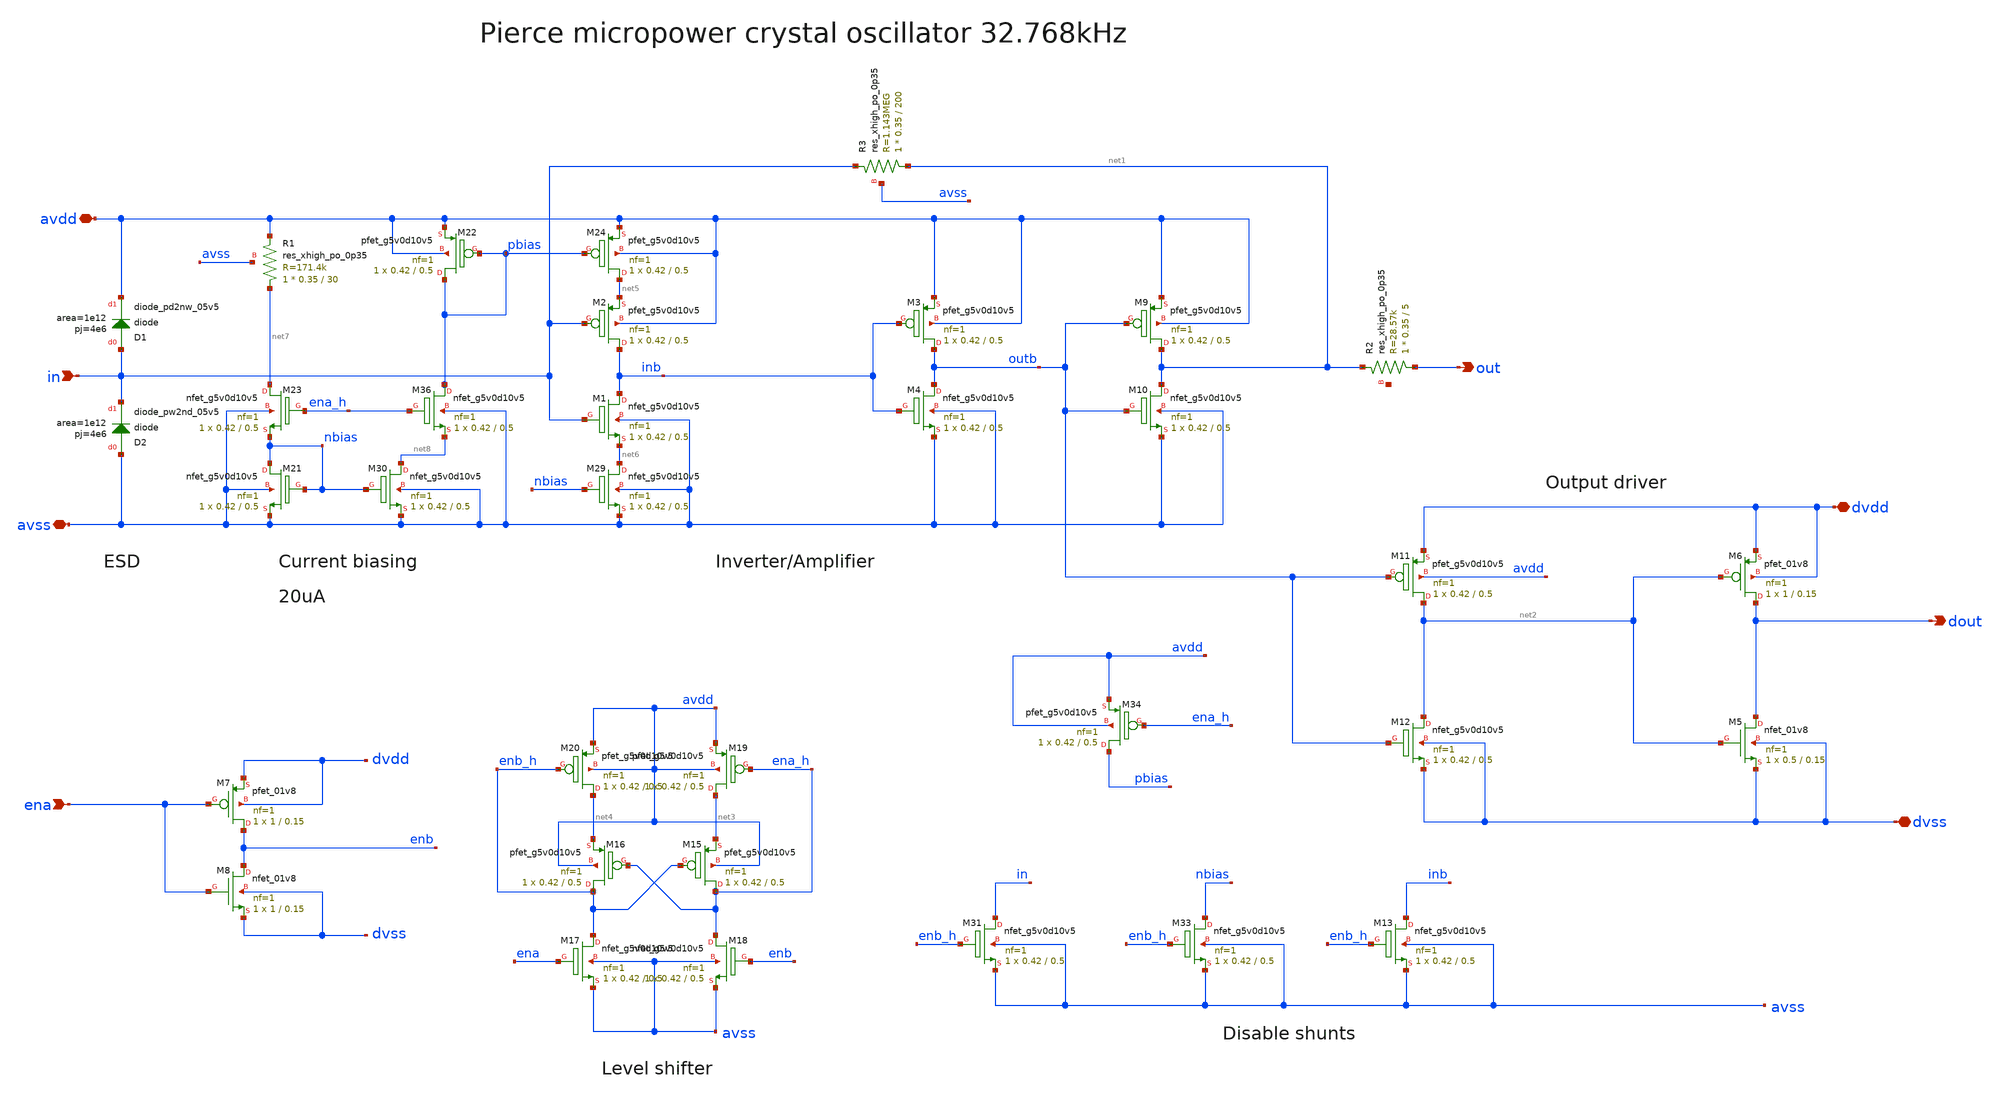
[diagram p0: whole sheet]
** sch_path: archive/pierce_xo.sch
**.subckt pierce_xo in out avdd avss dvss dvdd ena dout
*.ipin in
*.opin out
*.iopin avdd
*.iopin avss
*.iopin dvss
*.iopin dvdd
*.ipin ena
*.opin dout
XM1 inb in net6 avss sky130_fd_pr__nfet_g5v0d10v5 L=0.5 W=0.42 nf=1 ad='int((nf+1)/2) * W/nf * 0.29'
+ as='int((nf+2)/2) * W/nf * 0.29' pd='2*int((nf+1)/2) * (W/nf + 0.29)' ps='2*int((nf+2)/2) * (W/nf + 0.29)'
+ nrd='0.29 / W' nrs='0.29 / W' sa=0 sb=0 sd=0 mult=1 m=1
XM2 inb in net5 avdd sky130_fd_pr__pfet_g5v0d10v5 L=0.5 W=0.42 nf=1 ad='int((nf+1)/2) * W/nf * 0.29'
+ as='int((nf+2)/2) * W/nf * 0.29' pd='2*int((nf+1)/2) * (W/nf + 0.29)' ps='2*int((nf+2)/2) * (W/nf + 0.29)'
+ nrd='0.29 / W' nrs='0.29 / W' sa=0 sb=0 sd=0 mult=1 m=1
XM3 outb inb avdd avdd sky130_fd_pr__pfet_g5v0d10v5 L=0.5 W=0.42 nf=1 ad='int((nf+1)/2) * W/nf * 0.29'
+ as='int((nf+2)/2) * W/nf * 0.29' pd='2*int((nf+1)/2) * (W/nf + 0.29)' ps='2*int((nf+2)/2) * (W/nf + 0.29)'
+ nrd='0.29 / W' nrs='0.29 / W' sa=0 sb=0 sd=0 mult=1 m=1
XM4 outb inb avss avss sky130_fd_pr__nfet_g5v0d10v5 L=0.5 W=0.42 nf=1 ad='int((nf+1)/2) * W/nf * 0.29'
+ as='int((nf+2)/2) * W/nf * 0.29' pd='2*int((nf+1)/2) * (W/nf + 0.29)' ps='2*int((nf+2)/2) * (W/nf + 0.29)'
+ nrd='0.29 / W' nrs='0.29 / W' sa=0 sb=0 sd=0 mult=1 m=1
XM5 dout net2 dvss dvss sky130_fd_pr__nfet_01v8 L=0.15 W=0.5 nf=1 ad='int((nf+1)/2) * W/nf * 0.29' as='int((nf+2)/2) * W/nf * 0.29'
+ pd='2*int((nf+1)/2) * (W/nf + 0.29)' ps='2*int((nf+2)/2) * (W/nf + 0.29)' nrd='0.29 / W' nrs='0.29 / W'
+ sa=0 sb=0 sd=0 mult=1 m=1
XM6 dout net2 dvdd dvdd sky130_fd_pr__pfet_01v8 L=0.15 W=1 nf=1 ad='int((nf+1)/2) * W/nf * 0.29' as='int((nf+2)/2) * W/nf * 0.29'
+ pd='2*int((nf+1)/2) * (W/nf + 0.29)' ps='2*int((nf+2)/2) * (W/nf + 0.29)' nrd='0.29 / W' nrs='0.29 / W'
+ sa=0 sb=0 sd=0 mult=1 m=1
XM7 enb ena dvdd dvdd sky130_fd_pr__pfet_01v8 L=0.15 W=1 nf=1 ad='int((nf+1)/2) * W/nf * 0.29' as='int((nf+2)/2) * W/nf * 0.29'
+ pd='2*int((nf+1)/2) * (W/nf + 0.29)' ps='2*int((nf+2)/2) * (W/nf + 0.29)' nrd='0.29 / W' nrs='0.29 / W'
+ sa=0 sb=0 sd=0 mult=1 m=1
XM8 enb ena dvss dvss sky130_fd_pr__nfet_01v8 L=0.15 W=1 nf=1 ad='int((nf+1)/2) * W/nf * 0.29' as='int((nf+2)/2) * W/nf * 0.29'
+ pd='2*int((nf+1)/2) * (W/nf + 0.29)' ps='2*int((nf+2)/2) * (W/nf + 0.29)' nrd='0.29 / W' nrs='0.29 / W'
+ sa=0 sb=0 sd=0 mult=1 m=1
XR3 net1 in avss sky130_fd_pr__res_xhigh_po_0p35 L=200 mult=1 m=1
XM9 net1 outb avdd avdd sky130_fd_pr__pfet_g5v0d10v5 L=0.5 W=0.42 nf=1 ad='int((nf+1)/2) * W/nf * 0.29'
+ as='int((nf+2)/2) * W/nf * 0.29' pd='2*int((nf+1)/2) * (W/nf + 0.29)' ps='2*int((nf+2)/2) * (W/nf + 0.29)'
+ nrd='0.29 / W' nrs='0.29 / W' sa=0 sb=0 sd=0 mult=1 m=1
XM10 net1 outb avss avss sky130_fd_pr__nfet_g5v0d10v5 L=0.5 W=0.42 nf=1 ad='int((nf+1)/2) * W/nf * 0.29'
+ as='int((nf+2)/2) * W/nf * 0.29' pd='2*int((nf+1)/2) * (W/nf + 0.29)' ps='2*int((nf+2)/2) * (W/nf + 0.29)'
+ nrd='0.29 / W' nrs='0.29 / W' sa=0 sb=0 sd=0 mult=1 m=1
XM11 net2 outb dvdd avdd sky130_fd_pr__pfet_g5v0d10v5 L=0.5 W=0.42 nf=1 ad='int((nf+1)/2) * W/nf * 0.29'
+ as='int((nf+2)/2) * W/nf * 0.29' pd='2*int((nf+1)/2) * (W/nf + 0.29)' ps='2*int((nf+2)/2) * (W/nf + 0.29)'
+ nrd='0.29 / W' nrs='0.29 / W' sa=0 sb=0 sd=0 mult=1 m=1
XM12 net2 outb dvss dvss sky130_fd_pr__nfet_g5v0d10v5 L=0.5 W=0.42 nf=1 ad='int((nf+1)/2) * W/nf * 0.29'
+ as='int((nf+2)/2) * W/nf * 0.29' pd='2*int((nf+1)/2) * (W/nf + 0.29)' ps='2*int((nf+2)/2) * (W/nf + 0.29)'
+ nrd='0.29 / W' nrs='0.29 / W' sa=0 sb=0 sd=0 mult=1 m=1
XD1 in avdd sky130_fd_pr__diode_pd2nw_05v5 area=1e12 pj=4e6
XD2 avss in sky130_fd_pr__diode_pw2nd_05v5 area=1e12 pj=4e6
XM15 ena_h enb_h net3 avdd sky130_fd_pr__pfet_g5v0d10v5 L=0.5 W=0.42 nf=1 ad='int((nf+1)/2) * W/nf * 0.29'
+ as='int((nf+2)/2) * W/nf * 0.29' pd='2*int((nf+1)/2) * (W/nf + 0.29)' ps='2*int((nf+2)/2) * (W/nf + 0.29)'
+ nrd='0.29 / W' nrs='0.29 / W' sa=0 sb=0 sd=0 mult=1 m=1
XM16 enb_h ena_h net4 avdd sky130_fd_pr__pfet_g5v0d10v5 L=0.5 W=0.42 nf=1 ad='int((nf+1)/2) * W/nf * 0.29'
+ as='int((nf+2)/2) * W/nf * 0.29' pd='2*int((nf+1)/2) * (W/nf + 0.29)' ps='2*int((nf+2)/2) * (W/nf + 0.29)'
+ nrd='0.29 / W' nrs='0.29 / W' sa=0 sb=0 sd=0 mult=1 m=1
XM17 enb_h ena avss avss sky130_fd_pr__nfet_g5v0d10v5 L=0.5 W=0.42 nf=1 ad='int((nf+1)/2) * W/nf * 0.29'
+ as='int((nf+2)/2) * W/nf * 0.29' pd='2*int((nf+1)/2) * (W/nf + 0.29)' ps='2*int((nf+2)/2) * (W/nf + 0.29)'
+ nrd='0.29 / W' nrs='0.29 / W' sa=0 sb=0 sd=0 mult=1 m=1
XM18 ena_h enb avss avss sky130_fd_pr__nfet_g5v0d10v5 L=0.5 W=0.42 nf=1 ad='int((nf+1)/2) * W/nf * 0.29'
+ as='int((nf+2)/2) * W/nf * 0.29' pd='2*int((nf+1)/2) * (W/nf + 0.29)' ps='2*int((nf+2)/2) * (W/nf + 0.29)'
+ nrd='0.29 / W' nrs='0.29 / W' sa=0 sb=0 sd=0 mult=1 m=1
XM19 net3 ena_h avdd avdd sky130_fd_pr__pfet_g5v0d10v5 L=0.5 W=0.42 nf=1 ad='int((nf+1)/2) * W/nf * 0.29'
+ as='int((nf+2)/2) * W/nf * 0.29' pd='2*int((nf+1)/2) * (W/nf + 0.29)' ps='2*int((nf+2)/2) * (W/nf + 0.29)'
+ nrd='0.29 / W' nrs='0.29 / W' sa=0 sb=0 sd=0 mult=1 m=1
XM20 net4 enb_h avdd avdd sky130_fd_pr__pfet_g5v0d10v5 L=0.5 W=0.42 nf=1 ad='int((nf+1)/2) * W/nf * 0.29'
+ as='int((nf+2)/2) * W/nf * 0.29' pd='2*int((nf+1)/2) * (W/nf + 0.29)' ps='2*int((nf+2)/2) * (W/nf + 0.29)'
+ nrd='0.29 / W' nrs='0.29 / W' sa=0 sb=0 sd=0 mult=1 m=1
XM24 net5 pbias avdd avdd sky130_fd_pr__pfet_g5v0d10v5 L=0.5 W=0.42 nf=1 ad='int((nf+1)/2) * W/nf * 0.29'
+ as='int((nf+2)/2) * W/nf * 0.29' pd='2*int((nf+1)/2) * (W/nf + 0.29)' ps='2*int((nf+2)/2) * (W/nf + 0.29)'
+ nrd='0.29 / W' nrs='0.29 / W' sa=0 sb=0 sd=0 mult=1 m=1
XM29 net6 nbias avss avss sky130_fd_pr__nfet_g5v0d10v5 L=0.5 W=0.42 nf=1 ad='int((nf+1)/2) * W/nf * 0.29'
+ as='int((nf+2)/2) * W/nf * 0.29' pd='2*int((nf+1)/2) * (W/nf + 0.29)' ps='2*int((nf+2)/2) * (W/nf + 0.29)'
+ nrd='0.29 / W' nrs='0.29 / W' sa=0 sb=0 sd=0 mult=1 m=1
XM21 nbias nbias avss avss sky130_fd_pr__nfet_g5v0d10v5 L=0.5 W=0.42 nf=1 ad='int((nf+1)/2) * W/nf * 0.29'
+ as='int((nf+2)/2) * W/nf * 0.29' pd='2*int((nf+1)/2) * (W/nf + 0.29)' ps='2*int((nf+2)/2) * (W/nf + 0.29)'
+ nrd='0.29 / W' nrs='0.29 / W' sa=0 sb=0 sd=0 mult=1 m=1
XM22 pbias pbias avdd avdd sky130_fd_pr__pfet_g5v0d10v5 L=0.5 W=0.42 nf=1 ad='int((nf+1)/2) * W/nf * 0.29'
+ as='int((nf+2)/2) * W/nf * 0.29' pd='2*int((nf+1)/2) * (W/nf + 0.29)' ps='2*int((nf+2)/2) * (W/nf + 0.29)'
+ nrd='0.29 / W' nrs='0.29 / W' sa=0 sb=0 sd=0 mult=1 m=1
XR1 net7 avdd avss sky130_fd_pr__res_xhigh_po_0p35 L=30 mult=1 m=1
XM23 net7 ena_h nbias avss sky130_fd_pr__nfet_g5v0d10v5 L=0.5 W=0.42 nf=1 ad='int((nf+1)/2) * W/nf * 0.29'
+ as='int((nf+2)/2) * W/nf * 0.29' pd='2*int((nf+1)/2) * (W/nf + 0.29)' ps='2*int((nf+2)/2) * (W/nf + 0.29)'
+ nrd='0.29 / W' nrs='0.29 / W' sa=0 sb=0 sd=0 mult=1 m=1
XM30 net8 nbias avss avss sky130_fd_pr__nfet_g5v0d10v5 L=0.5 W=0.42 nf=1 ad='int((nf+1)/2) * W/nf * 0.29'
+ as='int((nf+2)/2) * W/nf * 0.29' pd='2*int((nf+1)/2) * (W/nf + 0.29)' ps='2*int((nf+2)/2) * (W/nf + 0.29)'
+ nrd='0.29 / W' nrs='0.29 / W' sa=0 sb=0 sd=0 mult=1 m=1
XM31 in enb_h avss avss sky130_fd_pr__nfet_g5v0d10v5 L=0.5 W=0.42 nf=1 ad='int((nf+1)/2) * W/nf * 0.29'
+ as='int((nf+2)/2) * W/nf * 0.29' pd='2*int((nf+1)/2) * (W/nf + 0.29)' ps='2*int((nf+2)/2) * (W/nf + 0.29)'
+ nrd='0.29 / W' nrs='0.29 / W' sa=0 sb=0 sd=0 mult=1 m=1
XM33 nbias enb_h avss avss sky130_fd_pr__nfet_g5v0d10v5 L=0.5 W=0.42 nf=1 ad='int((nf+1)/2) * W/nf * 0.29'
+ as='int((nf+2)/2) * W/nf * 0.29' pd='2*int((nf+1)/2) * (W/nf + 0.29)' ps='2*int((nf+2)/2) * (W/nf + 0.29)'
+ nrd='0.29 / W' nrs='0.29 / W' sa=0 sb=0 sd=0 mult=1 m=1
XM34 pbias ena_h avdd avdd sky130_fd_pr__pfet_g5v0d10v5 L=0.5 W=0.42 nf=1 ad='int((nf+1)/2) * W/nf * 0.29'
+ as='int((nf+2)/2) * W/nf * 0.29' pd='2*int((nf+1)/2) * (W/nf + 0.29)' ps='2*int((nf+2)/2) * (W/nf + 0.29)'
+ nrd='0.29 / W' nrs='0.29 / W' sa=0 sb=0 sd=0 mult=1 m=1
XM36 pbias ena_h net8 avss sky130_fd_pr__nfet_g5v0d10v5 L=0.5 W=0.42 nf=1 ad='int((nf+1)/2) * W/nf * 0.29'
+ as='int((nf+2)/2) * W/nf * 0.29' pd='2*int((nf+1)/2) * (W/nf + 0.29)' ps='2*int((nf+2)/2) * (W/nf + 0.29)'
+ nrd='0.29 / W' nrs='0.29 / W' sa=0 sb=0 sd=0 mult=1 m=1
XM13 inb enb_h avss avss sky130_fd_pr__nfet_g5v0d10v5 L=0.5 W=0.42 nf=1 ad='int((nf+1)/2) * W/nf * 0.29'
+ as='int((nf+2)/2) * W/nf * 0.29' pd='2*int((nf+1)/2) * (W/nf + 0.29)' ps='2*int((nf+2)/2) * (W/nf + 0.29)'
+ nrd='0.29 / W' nrs='0.29 / W' sa=0 sb=0 sd=0 mult=1 m=1
XR2 out net1 net9 sky130_fd_pr__res_xhigh_po_0p35 L=5 mult=1 m=1
**.ends
.end
